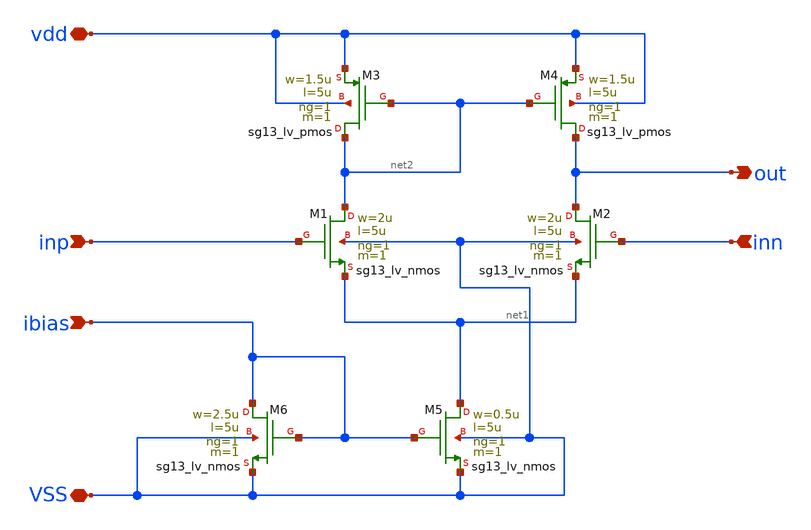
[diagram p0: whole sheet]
** sch_path: 3_Real_Cir/basic_5t_ota.sch
**.subckt basic_5t_ota vdd ibias inp VSS inn out
*.iopin vdd
*.ipin ibias
*.ipin inp
*.iopin VSS
*.ipin inn
*.opin out
XM1 net2 inp net1 VSS sg13_lv_nmos w=2u l=5u ng=1 m=1 mm_ok=1
XM2 out inn net1 VSS sg13_lv_nmos w=2u l=5u ng=1 m=1 mm_ok=1
XM3 net2 net2 vdd vdd sg13_lv_pmos w=1.5u l=5u ng=1 m=1 mm_ok=1
XM4 out net2 vdd vdd sg13_lv_pmos w=1.5u l=5u ng=1 m=1 mm_ok=1
XM5 net1 ibias VSS VSS sg13_lv_nmos w=0.5u l=5u ng=1 m=1 mm_ok=1
XM6 ibias ibias VSS VSS sg13_lv_nmos w=2.5u l=5u ng=1 m=1 mm_ok=1
**.ends
.end
